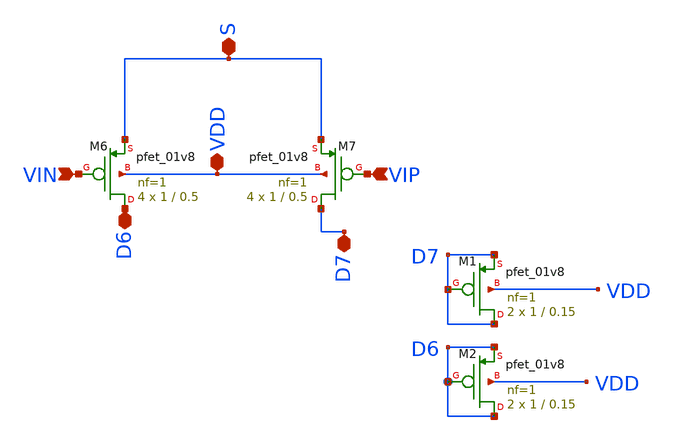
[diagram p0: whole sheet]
** sch_path: opamp/xschem/pmosdif.sch
**.subckt pmosdif S D6 VDD D7 VIP VIN
*.iopin S
*.iopin D6
*.iopin VDD
*.iopin D7
*.ipin VIP
*.ipin VIN
XM6 D6 VIN S VDD sky130_fd_pr__pfet_01v8 L=0.5 W=1 nf=1 ad='int((nf+1)/2) * W/nf * 0.29' as='int((nf+2)/2) * W/nf * 0.29'
+ pd='2*int((nf+1)/2) * (W/nf + 0.29)' ps='2*int((nf+2)/2) * (W/nf + 0.29)' nrd='0.29 / W' nrs='0.29 / W'
+ sa=0 sb=0 sd=0 mult=4 m=4
XM7 D7 VIP S VDD sky130_fd_pr__pfet_01v8 L=0.5 W=1 nf=1 ad='int((nf+1)/2) * W/nf * 0.29' as='int((nf+2)/2) * W/nf * 0.29'
+ pd='2*int((nf+1)/2) * (W/nf + 0.29)' ps='2*int((nf+2)/2) * (W/nf + 0.29)' nrd='0.29 / W' nrs='0.29 / W'
+ sa=0 sb=0 sd=0 mult=4 m=4
XM1 D7 D7 D7 VDD sky130_fd_pr__pfet_01v8 L=0.15 W=1 nf=1 ad='int((nf+1)/2) * W/nf * 0.29' as='int((nf+2)/2) * W/nf * 0.29'
+ pd='2*int((nf+1)/2) * (W/nf + 0.29)' ps='2*int((nf+2)/2) * (W/nf + 0.29)' nrd='0.29 / W' nrs='0.29 / W'
+ sa=0 sb=0 sd=0 mult=2 m=2
XM2 D6 D6 D6 VDD sky130_fd_pr__pfet_01v8 L=0.15 W=1 nf=1 ad='int((nf+1)/2) * W/nf * 0.29' as='int((nf+2)/2) * W/nf * 0.29'
+ pd='2*int((nf+1)/2) * (W/nf + 0.29)' ps='2*int((nf+2)/2) * (W/nf + 0.29)' nrd='0.29 / W' nrs='0.29 / W'
+ sa=0 sb=0 sd=0 mult=2 m=2
**.ends
.end
